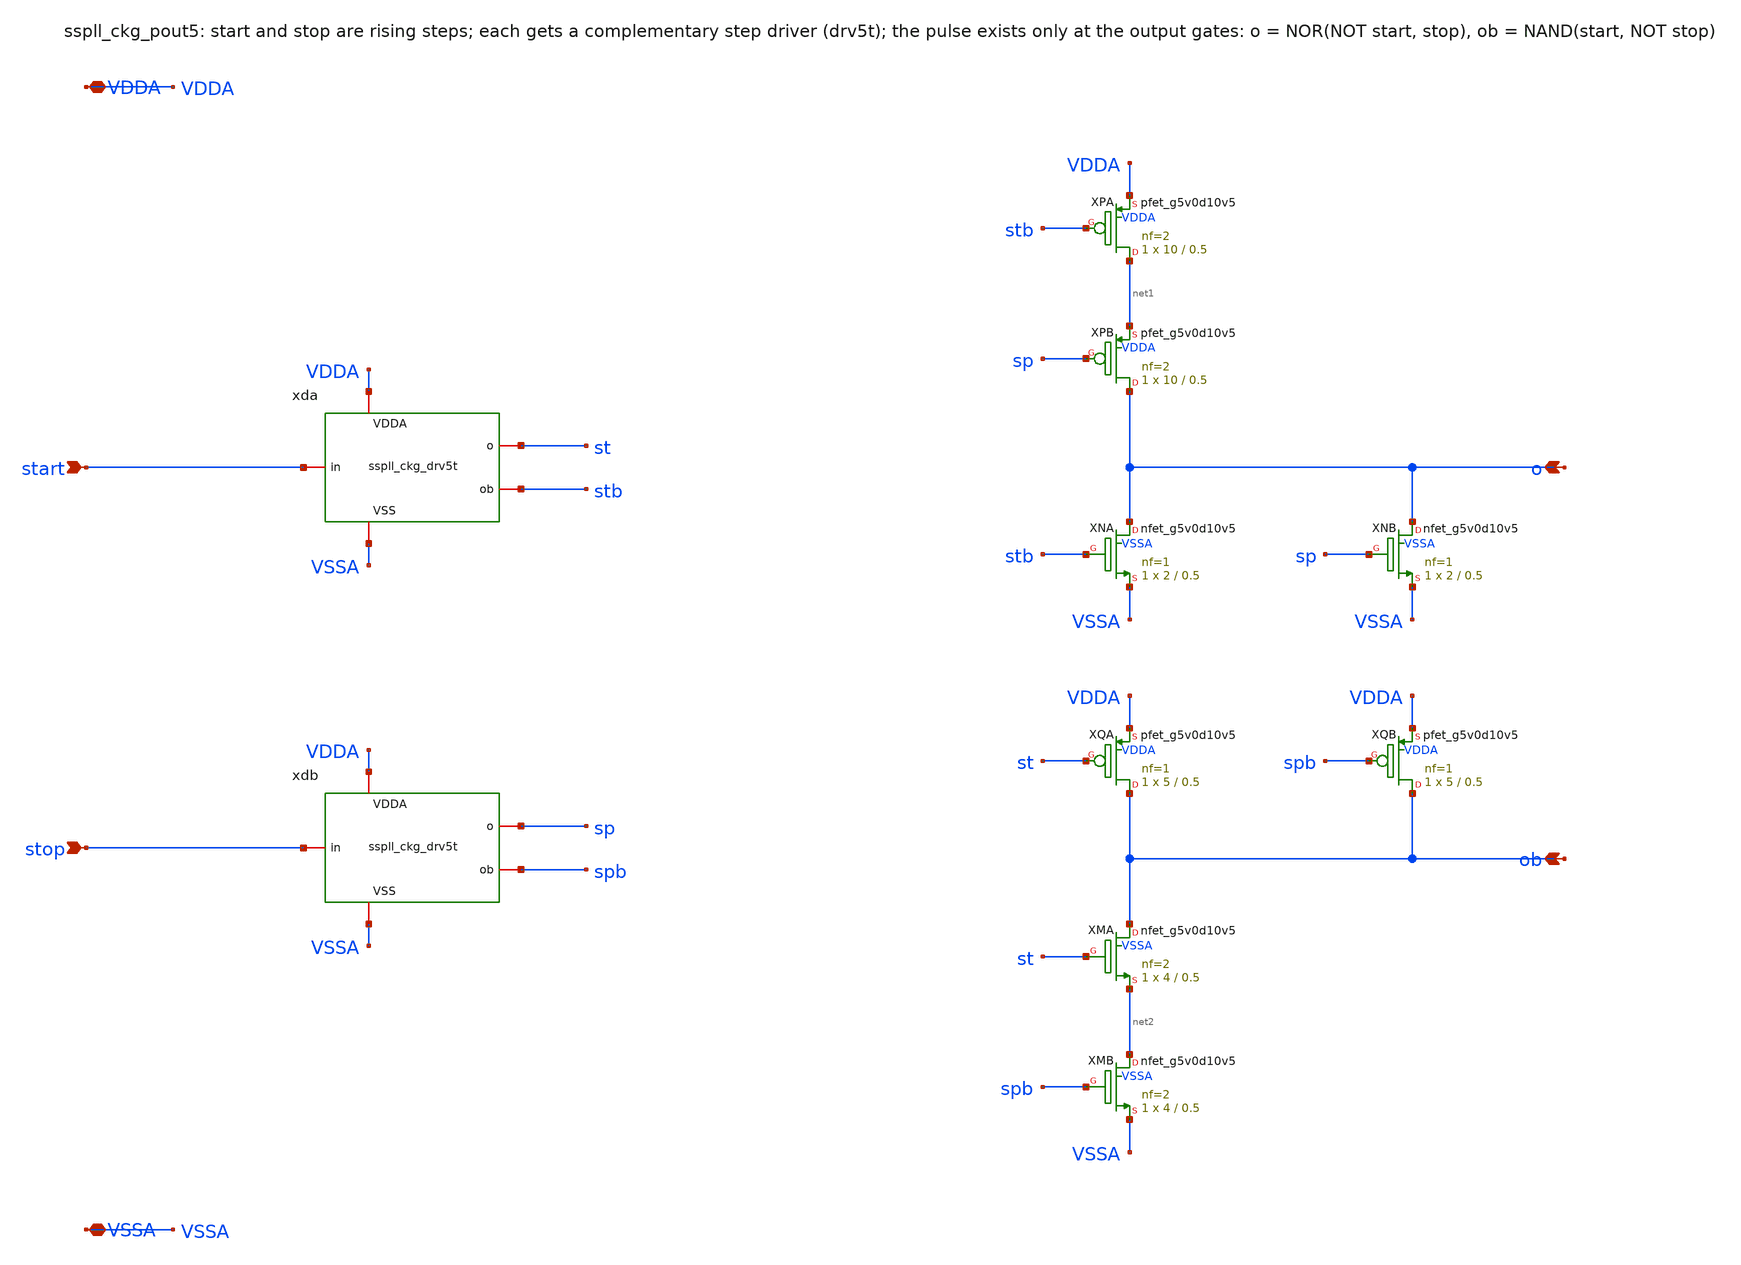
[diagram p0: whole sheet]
** sch_path: xschem/clkgen_hv/sspll_ckg_pout5.sch
**.subckt sspll_ckg_pout5 start stop o ob VDDA VSSA
*.ipin start
*.ipin stop
*.opin o
*.opin ob
*.iopin VDDA
*.iopin VSSA
xda start st stb VDDA VSSA sspll_ckg_drv5t
xdb stop sp spb VDDA VSSA sspll_ckg_drv5t
XXPA net1 stb VDDA VDDA sky130_fd_pr__pfet_g5v0d10v5 L=0.5 W=10 nf=2 ad='int((nf+1)/2) * W/nf * 0.29'
+ as='int((nf+2)/2) * W/nf * 0.29' pd='2*int((nf+1)/2) * (W/nf + 0.29)' ps='2*int((nf+2)/2) * (W/nf + 0.29)'
+ nrd='0.29 / W' nrs='0.29 / W' sa=0 sb=0 sd=0 mult=1 m=1
XXPB o sp net1 VDDA sky130_fd_pr__pfet_g5v0d10v5 L=0.5 W=10 nf=2 ad='int((nf+1)/2) * W/nf * 0.29' as='int((nf+2)/2) * W/nf * 0.29'
+ pd='2*int((nf+1)/2) * (W/nf + 0.29)' ps='2*int((nf+2)/2) * (W/nf + 0.29)' nrd='0.29 / W' nrs='0.29 / W'
+ sa=0 sb=0 sd=0 mult=1 m=1
XXNA o stb VSSA VSSA sky130_fd_pr__nfet_g5v0d10v5 L=0.5 W=2 nf=1 ad='int((nf+1)/2) * W/nf * 0.29' as='int((nf+2)/2) * W/nf * 0.29'
+ pd='2*int((nf+1)/2) * (W/nf + 0.29)' ps='2*int((nf+2)/2) * (W/nf + 0.29)' nrd='0.29 / W' nrs='0.29 / W'
+ sa=0 sb=0 sd=0 mult=1 m=1
XXNB o sp VSSA VSSA sky130_fd_pr__nfet_g5v0d10v5 L=0.5 W=2 nf=1 ad='int((nf+1)/2) * W/nf * 0.29' as='int((nf+2)/2) * W/nf * 0.29'
+ pd='2*int((nf+1)/2) * (W/nf + 0.29)' ps='2*int((nf+2)/2) * (W/nf + 0.29)' nrd='0.29 / W' nrs='0.29 / W'
+ sa=0 sb=0 sd=0 mult=1 m=1
XXQA ob st VDDA VDDA sky130_fd_pr__pfet_g5v0d10v5 L=0.5 W=5 nf=1 ad='int((nf+1)/2) * W/nf * 0.29' as='int((nf+2)/2) * W/nf * 0.29'
+ pd='2*int((nf+1)/2) * (W/nf + 0.29)' ps='2*int((nf+2)/2) * (W/nf + 0.29)' nrd='0.29 / W' nrs='0.29 / W'
+ sa=0 sb=0 sd=0 mult=1 m=1
XXQB ob spb VDDA VDDA sky130_fd_pr__pfet_g5v0d10v5 L=0.5 W=5 nf=1 ad='int((nf+1)/2) * W/nf * 0.29' as='int((nf+2)/2) * W/nf * 0.29'
+ pd='2*int((nf+1)/2) * (W/nf + 0.29)' ps='2*int((nf+2)/2) * (W/nf + 0.29)' nrd='0.29 / W' nrs='0.29 / W'
+ sa=0 sb=0 sd=0 mult=1 m=1
XXMA ob st net2 VSSA sky130_fd_pr__nfet_g5v0d10v5 L=0.5 W=4 nf=2 ad='int((nf+1)/2) * W/nf * 0.29' as='int((nf+2)/2) * W/nf * 0.29'
+ pd='2*int((nf+1)/2) * (W/nf + 0.29)' ps='2*int((nf+2)/2) * (W/nf + 0.29)' nrd='0.29 / W' nrs='0.29 / W'
+ sa=0 sb=0 sd=0 mult=1 m=1
XXMB net2 spb VSSA VSSA sky130_fd_pr__nfet_g5v0d10v5 L=0.5 W=4 nf=2 ad='int((nf+1)/2) * W/nf * 0.29'
+ as='int((nf+2)/2) * W/nf * 0.29' pd='2*int((nf+1)/2) * (W/nf + 0.29)' ps='2*int((nf+2)/2) * (W/nf + 0.29)'
+ nrd='0.29 / W' nrs='0.29 / W' sa=0 sb=0 sd=0 mult=1 m=1
**.ends

* expanding   symbol:  sspll_ckg_drv5t.sym # of pins=5
** sym_path: xschem/clkgen_hv/sspll_ckg_drv5t.sym
** sch_path: xschem/clkgen_hv/sspll_ckg_drv5t.sch
.subckt sspll_ckg_drv5t in o ob VDDA VSS
*.ipin in
*.opin o
*.opin ob
*.iopin VDDA
*.iopin VSS
XXTN net1 VDDA in VSS sky130_fd_pr__nfet_g5v0d10v5 L=0.5 W=0.75 nf=1 ad='int((nf+1)/2) * W/nf * 0.29'
+ as='int((nf+2)/2) * W/nf * 0.29' pd='2*int((nf+1)/2) * (W/nf + 0.29)' ps='2*int((nf+2)/2) * (W/nf + 0.29)'
+ nrd='0.29 / W' nrs='0.29 / W' sa=0 sb=0 sd=0 mult=1 m=1
XXTP net1 VSS in VDDA sky130_fd_pr__pfet_g5v0d10v5 L=0.5 W=0.75 nf=1 ad='int((nf+1)/2) * W/nf * 0.29'
+ as='int((nf+2)/2) * W/nf * 0.29' pd='2*int((nf+1)/2) * (W/nf + 0.29)' ps='2*int((nf+2)/2) * (W/nf + 0.29)'
+ nrd='0.29 / W' nrs='0.29 / W' sa=0 sb=0 sd=0 mult=1 m=1
XXAP net2 net1 VDDA VDDA sky130_fd_pr__pfet_g5v0d10v5 L=0.5 W=6.25 nf=1 ad='int((nf+1)/2) * W/nf * 0.29'
+ as='int((nf+2)/2) * W/nf * 0.29' pd='2*int((nf+1)/2) * (W/nf + 0.29)' ps='2*int((nf+2)/2) * (W/nf + 0.29)'
+ nrd='0.29 / W' nrs='0.29 / W' sa=0 sb=0 sd=0 mult=1 m=1
XXAN net2 net1 VSS VSS sky130_fd_pr__nfet_g5v0d10v5 L=0.5 W=2.5 nf=1 ad='int((nf+1)/2) * W/nf * 0.29'
+ as='int((nf+2)/2) * W/nf * 0.29' pd='2*int((nf+1)/2) * (W/nf + 0.29)' ps='2*int((nf+2)/2) * (W/nf + 0.29)'
+ nrd='0.29 / W' nrs='0.29 / W' sa=0 sb=0 sd=0 mult=1 m=1
XXBP o net2 VDDA VDDA sky130_fd_pr__pfet_g5v0d10v5 L=0.5 W=5 nf=1 ad='int((nf+1)/2) * W/nf * 0.29' as='int((nf+2)/2) * W/nf * 0.29'
+ pd='2*int((nf+1)/2) * (W/nf + 0.29)' ps='2*int((nf+2)/2) * (W/nf + 0.29)' nrd='0.29 / W' nrs='0.29 / W'
+ sa=0 sb=0 sd=0 mult=1 m=1
XXBN o net2 VSS VSS sky130_fd_pr__nfet_g5v0d10v5 L=0.5 W=2 nf=1 ad='int((nf+1)/2) * W/nf * 0.29' as='int((nf+2)/2) * W/nf * 0.29'
+ pd='2*int((nf+1)/2) * (W/nf + 0.29)' ps='2*int((nf+2)/2) * (W/nf + 0.29)' nrd='0.29 / W' nrs='0.29 / W'
+ sa=0 sb=0 sd=0 mult=1 m=1
XXCP net3 in VDDA VDDA sky130_fd_pr__pfet_g5v0d10v5 L=0.5 W=2.5 nf=1 ad='int((nf+1)/2) * W/nf * 0.29'
+ as='int((nf+2)/2) * W/nf * 0.29' pd='2*int((nf+1)/2) * (W/nf + 0.29)' ps='2*int((nf+2)/2) * (W/nf + 0.29)'
+ nrd='0.29 / W' nrs='0.29 / W' sa=0 sb=0 sd=0 mult=1 m=1
XXCN net3 in VSS VSS sky130_fd_pr__nfet_g5v0d10v5 L=0.5 W=1 nf=1 ad='int((nf+1)/2) * W/nf * 0.29' as='int((nf+2)/2) * W/nf * 0.29'
+ pd='2*int((nf+1)/2) * (W/nf + 0.29)' ps='2*int((nf+2)/2) * (W/nf + 0.29)' nrd='0.29 / W' nrs='0.29 / W'
+ sa=0 sb=0 sd=0 mult=1 m=1
XXDP net4 net3 VDDA VDDA sky130_fd_pr__pfet_g5v0d10v5 L=0.5 W=6.25 nf=1 ad='int((nf+1)/2) * W/nf * 0.29'
+ as='int((nf+2)/2) * W/nf * 0.29' pd='2*int((nf+1)/2) * (W/nf + 0.29)' ps='2*int((nf+2)/2) * (W/nf + 0.29)'
+ nrd='0.29 / W' nrs='0.29 / W' sa=0 sb=0 sd=0 mult=1 m=1
XXDN net4 net3 VSS VSS sky130_fd_pr__nfet_g5v0d10v5 L=0.5 W=2.5 nf=1 ad='int((nf+1)/2) * W/nf * 0.29'
+ as='int((nf+2)/2) * W/nf * 0.29' pd='2*int((nf+1)/2) * (W/nf + 0.29)' ps='2*int((nf+2)/2) * (W/nf + 0.29)'
+ nrd='0.29 / W' nrs='0.29 / W' sa=0 sb=0 sd=0 mult=1 m=1
XXEP ob net4 VDDA VDDA sky130_fd_pr__pfet_g5v0d10v5 L=0.5 W=5 nf=1 ad='int((nf+1)/2) * W/nf * 0.29' as='int((nf+2)/2) * W/nf * 0.29'
+ pd='2*int((nf+1)/2) * (W/nf + 0.29)' ps='2*int((nf+2)/2) * (W/nf + 0.29)' nrd='0.29 / W' nrs='0.29 / W'
+ sa=0 sb=0 sd=0 mult=1 m=1
XXEN ob net4 VSS VSS sky130_fd_pr__nfet_g5v0d10v5 L=0.5 W=2 nf=1 ad='int((nf+1)/2) * W/nf * 0.29' as='int((nf+2)/2) * W/nf * 0.29'
+ pd='2*int((nf+1)/2) * (W/nf + 0.29)' ps='2*int((nf+2)/2) * (W/nf + 0.29)' nrd='0.29 / W' nrs='0.29 / W'
+ sa=0 sb=0 sd=0 mult=1 m=1
.ends

.end
